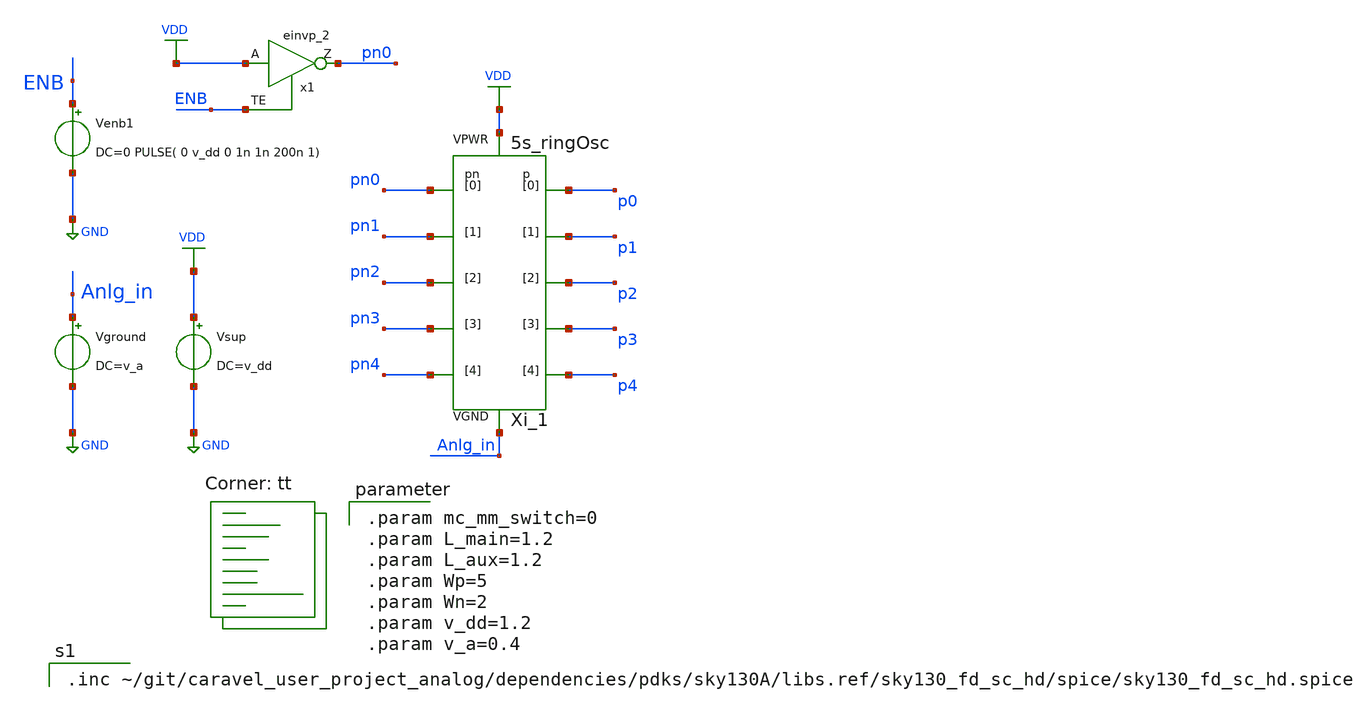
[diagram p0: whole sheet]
** sch_path: xschem/tb/5s_ringOsc_tb.sch
**.subckt 5s_ringOsc_tb
Vsup VDD GND DC=v_dd
Vground Anlg_in GND DC=v_a
Venb1 ENB GND DC=0 PULSE( 0 v_dd 0 1n 1n 200n 1)
Xi_1 Anlg_in VDD p0 p1 p2 p3 p4 pn0 pn1 pn2 pn3 pn4 5s_ringOsc L_main="L_main" L_aux="L_aux" Wp="Wp"
+ Wn="Wn"
x1 VDD ENB GND GND VDD VDD pn0 sky130_fd_sc_hd__einvp_2
**** begin user architecture code


.control
set nobreak
set num_threads=6
set test_mode = 0
* mode = 0: operation testing				1:  frequency extraction    2:  power consumption
if ($test_mode = 0)
    save all
    TRAN 10n 500u
    plot p0
    MEAS TRAN prd TRIG p0 VAL=0.8 RISE=10 TARG p0 VAL=0.8 RISE=20
    let freq = 10/prd
    echo "frequency: "
    print freq
end
if ($test_mode = 1)
    let Vlow = 0
    let Vlimit = 1.01     $ set upper bound for sweeping
    let Vsweep = 0.2      $ set step size for sweeping
    let NoPoints=(Vlimit-Vlow)/Vsweep+2    $ set number of points for sweeping
    let freq =unitvec(NoPoints)
    let Vin  =unitvec(NoPoints)
    let Vin[0]=Vlow
    let ix=0
    while Vin[ix] < Vlimit
        alter Vground DC=Vin[ix]
        TRAN 0.4n 12u
        MEAS TRAN prd TRIG pha_vco VAL=0.8 RISE=10 TARG pha_vco VAL=0.8 RISE =20
        let freq[ix] = 10/prd
        let ix = ix+1
        Let Vin[ix] = Vin[ix-1]+Vsweep
    end
   print Vin freq
end
if ($test_mode = 2)
    save "vdd" @Vsup[i] "p[0]"
    TRAN 0.1n 5u
    MEAS TRAN I_vco AVG @Vsup[i] FROM=3u TO=4u
    MEAS TRAN V_vco AVG vdd FROM=3u TO=4u
    let Power=I_vco*V_vco
    print Power
end
.endc



.param mc_mm_switch=0
.param L_main=1.2
.param L_aux=1.2
.param Wp=5
.param Wn=2
.param v_dd=1.2
.param v_a=0.4

.lib $::SKYWATER_MODELS/sky130.lib.spice tt

.inc ~/git/caravel_user_project_analog/dependencies/pdks/sky130A/libs.ref/sky130_fd_sc_hd/spice/sky130_fd_sc_hd.spice

**** end user architecture code
**.ends
.GLOBAL VDD
.GLOBAL GND
.end
